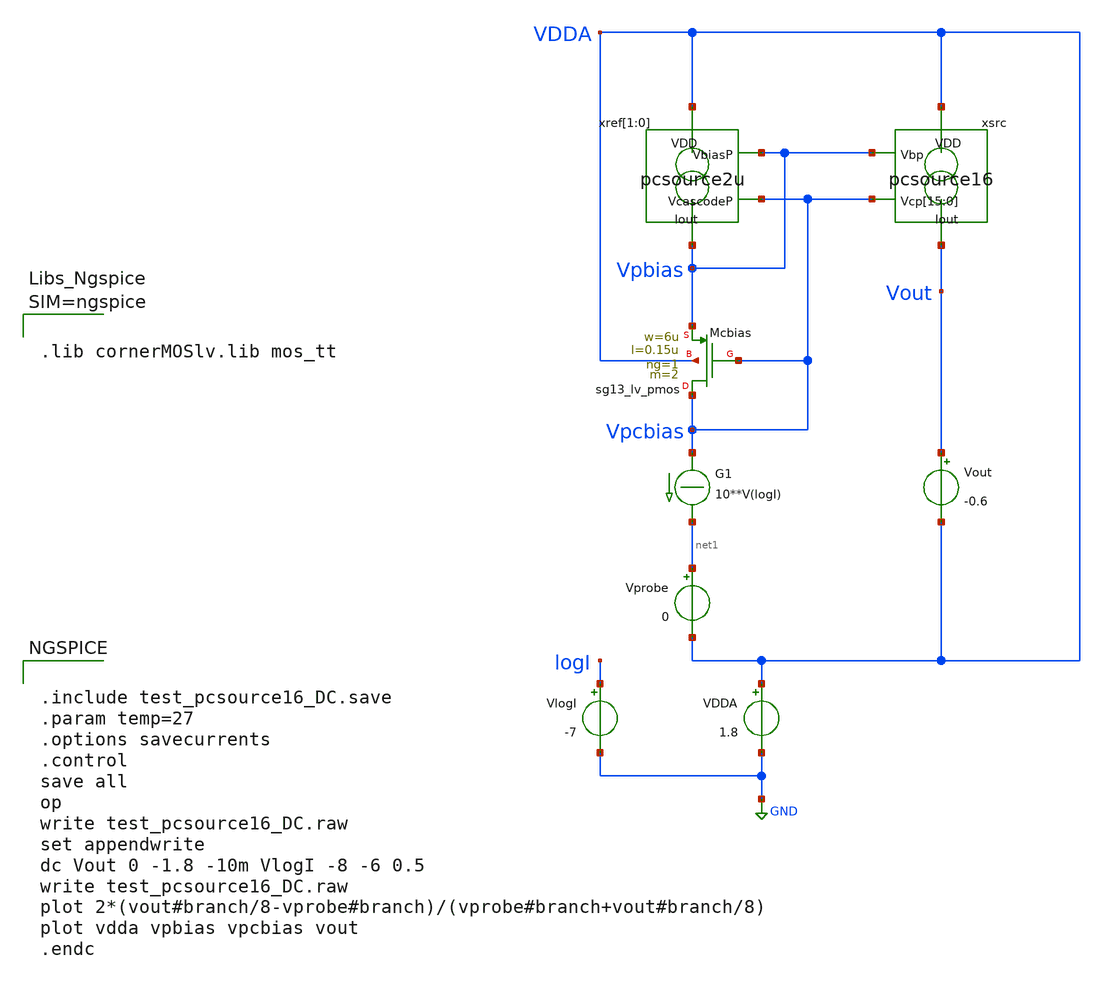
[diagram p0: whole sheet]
** sch_path: xschem/test_pcsource16_DC.sch
**.subckt test_pcsource16_DC
Vout Vout VDDA -0.6
.save i(vout)
Vprobe net1 VDDA 0
.save i(vprobe)
G1 Vpcbias net1 CUR=' 10**V(logI) '
VlogI logI GND -7
.save i(vlogi)
xref[1] VDDA Vpbias Vpcbias Vpbias pcsource2u
xref[0] VDDA Vpbias Vpcbias Vpbias pcsource2u
xsrc VDDA Vpbias Vpcbias Vpcbias Vpcbias Vpcbias Vpcbias Vpcbias Vpcbias Vpcbias Vpcbias Vpcbias
+ Vpcbias Vpcbias Vpcbias Vpcbias Vpcbias Vpcbias Vout pcsource16
VDDA VDDA GND 1.8
.save i(vdda)
XMcbias Vpcbias Vpcbias Vpbias VDDA sg13_lv_pmos w=6u l=0.15u ng=1 m=2 mm_ok=1
**** begin user architecture code


.include test_pcsource16_DC.save
.param temp=27
.options savecurrents
.control
save all
op
write test_pcsource16_DC.raw
set appendwrite
dc Vout 0 -1.8 -10m VlogI -8 -6 0.5
write test_pcsource16_DC.raw
plot 2*(vout#branch/8-vprobe#branch)/(vprobe#branch+vout#branch/8)
plot vdda vpbias vpcbias vout
.endc





.lib cornerMOSlv.lib mos_tt



**** end user architecture code
**.ends

* expanding   symbol:  pcsource2u.sym # of pins=4
** sym_path: xschem/pcsource2u.sym
** sch_path: xschem/pcsource2u.sch
.subckt pcsource2u VDD VbiasP VcascodeP Iout
*.ipin VcascodeP
*.ipin VbiasP
*.opin Iout
*.ipin VDD
XMsrc drain net4 VDD net1 sg13_lv_pmos w=1.45u l=5u ng=1 m=1 mm_ok=1
XMcasc Iout net3 drain net2 sg13_lv_pmos w=1.2u l=0.6u ng=1 m=1 mm_ok=1
Vgsrc net4 VbiasP 0
.save i(vgsrc)
Vgcasc net3 VcascodeP 0
.save i(vgcasc)
Vbsrc VDD net1 0
.save i(vbsrc)
Vbcasc VDD net2 0
.save i(vbcasc)
.ends


* expanding   symbol:  pcsource16.sym # of pins=4
** sym_path: xschem/pcsource16.sym
** sch_path: xschem/pcsource16.sch
.subckt pcsource16 VDD Vbp Vcp[15] Vcp[14] Vcp[13] Vcp[12] Vcp[11] Vcp[10] Vcp[9] Vcp[8] Vcp[7]
+ Vcp[6] Vcp[5] Vcp[4] Vcp[3] Vcp[2] Vcp[1] Vcp[0] Iout
*.ipin
*+ Vcp[15],Vcp[14],Vcp[13],Vcp[12],Vcp[11],Vcp[10],Vcp[9],Vcp[8],Vcp[7],Vcp[6],Vcp[5],Vcp[4],Vcp[3],Vcp[2],Vcp[1],Vcp[0]
*.ipin Vbp
*.opin Iout
*.ipin VDD
xsrc[15] VDD Vbp Vcp[15] Iout pcsource2u
xsrc[14] VDD Vbp Vcp[14] Iout pcsource2u
xsrc[13] VDD Vbp Vcp[13] Iout pcsource2u
xsrc[12] VDD Vbp Vcp[12] Iout pcsource2u
xsrc[11] VDD Vbp Vcp[11] Iout pcsource2u
xsrc[10] VDD Vbp Vcp[10] Iout pcsource2u
xsrc[9] VDD Vbp Vcp[9] Iout pcsource2u
xsrc[8] VDD Vbp Vcp[8] Iout pcsource2u
xsrc[7] VDD Vbp Vcp[7] Iout pcsource2u
xsrc[6] VDD Vbp Vcp[6] Iout pcsource2u
xsrc[5] VDD Vbp Vcp[5] Iout pcsource2u
xsrc[4] VDD Vbp Vcp[4] Iout pcsource2u
xsrc[3] VDD Vbp Vcp[3] Iout pcsource2u
xsrc[2] VDD Vbp Vcp[2] Iout pcsource2u
xsrc[1] VDD Vbp Vcp[1] Iout pcsource2u
xsrc[0] VDD Vbp Vcp[0] Iout pcsource2u
.ends

.GLOBAL GND
.end
